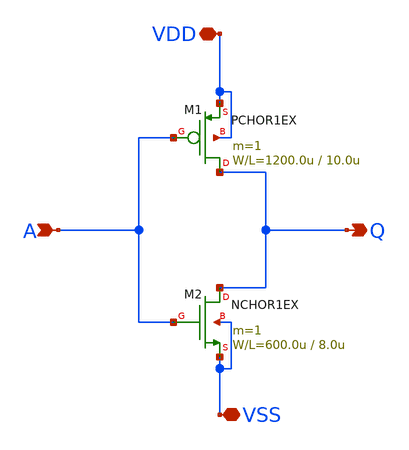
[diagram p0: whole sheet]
** sch_path: member_project/SIProp/large_inverter.sch
**.subckt large_inverter A Q VDD VSS
*.ipin A
*.opin Q
*.iopin VDD
*.iopin VSS
M2 Q A VSS VSS NCHOR1EX L=8.0u W=600.0u m=1
M1 Q A VDD VDD PCHOR1EX L=10.0u W=1200.0u m=1
**.ends
.end
